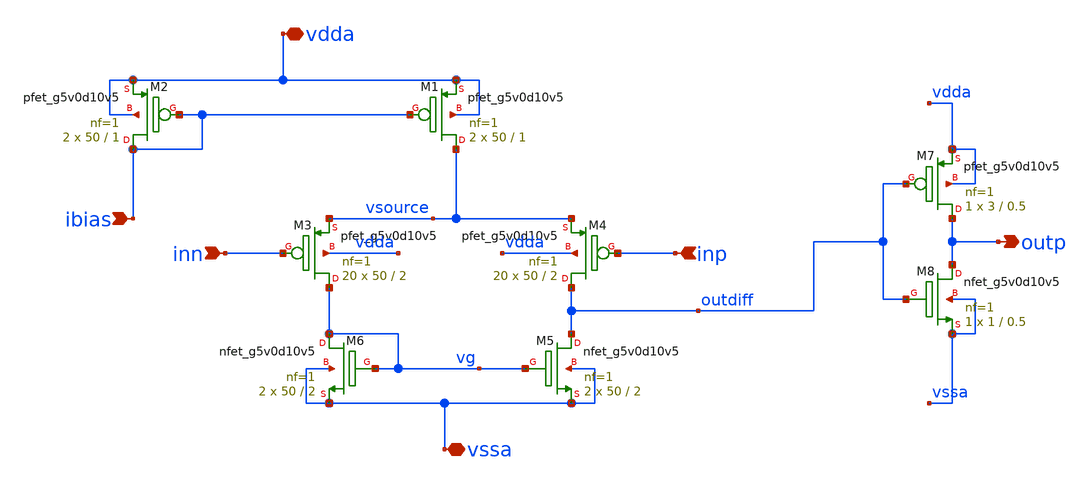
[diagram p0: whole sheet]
** sch_path: xschem/comparator1.sch
**.subckt comparator1 ibias inn inp vdda vssa outp
*.ipin ibias
*.ipin inn
*.ipin inp
*.iopin vdda
*.iopin vssa
*.opin outp
XM1 vsource ibias vdda vdda sky130_fd_pr__pfet_g5v0d10v5 L=1 W=50 nf=1 ad='int((nf+1)/2) * W/nf * 0.29'
+ as='int((nf+2)/2) * W/nf * 0.29' pd='2*int((nf+1)/2) * (W/nf + 0.29)' ps='2*int((nf+2)/2) * (W/nf + 0.29)'
+ nrd='0.29 / W' nrs='0.29 / W' sa=0 sb=0 sd=0 mult=2 m=2
XM2 ibias ibias vdda vdda sky130_fd_pr__pfet_g5v0d10v5 L=1 W=50 nf=1 ad='int((nf+1)/2) * W/nf * 0.29'
+ as='int((nf+2)/2) * W/nf * 0.29' pd='2*int((nf+1)/2) * (W/nf + 0.29)' ps='2*int((nf+2)/2) * (W/nf + 0.29)'
+ nrd='0.29 / W' nrs='0.29 / W' sa=0 sb=0 sd=0 mult=2 m=2
XM3 vg inn vsource vdda sky130_fd_pr__pfet_g5v0d10v5 L=2 W=50 nf=1 ad='int((nf+1)/2) * W/nf * 0.29' as='int((nf+2)/2) * W/nf * 0.29'
+ pd='2*int((nf+1)/2) * (W/nf + 0.29)' ps='2*int((nf+2)/2) * (W/nf + 0.29)' nrd='0.29 / W' nrs='0.29 / W'
+ sa=0 sb=0 sd=0 mult=20 m=20
XM4 outdiff inp vsource vdda sky130_fd_pr__pfet_g5v0d10v5 L=2 W=50 nf=1 ad='int((nf+1)/2) * W/nf * 0.29'
+ as='int((nf+2)/2) * W/nf * 0.29' pd='2*int((nf+1)/2) * (W/nf + 0.29)' ps='2*int((nf+2)/2) * (W/nf + 0.29)'
+ nrd='0.29 / W' nrs='0.29 / W' sa=0 sb=0 sd=0 mult=20 m=20
XM5 outdiff vg vssa vssa sky130_fd_pr__nfet_g5v0d10v5 L=2 W=50 nf=1 ad='int((nf+1)/2) * W/nf * 0.29'
+ as='int((nf+2)/2) * W/nf * 0.29' pd='2*int((nf+1)/2) * (W/nf + 0.29)' ps='2*int((nf+2)/2) * (W/nf + 0.29)'
+ nrd='0.29 / W' nrs='0.29 / W' sa=0 sb=0 sd=0 mult=2 m=2
XM6 vg vg vssa vssa sky130_fd_pr__nfet_g5v0d10v5 L=2 W=50 nf=1 ad='int((nf+1)/2) * W/nf * 0.29' as='int((nf+2)/2) * W/nf * 0.29'
+ pd='2*int((nf+1)/2) * (W/nf + 0.29)' ps='2*int((nf+2)/2) * (W/nf + 0.29)' nrd='0.29 / W' nrs='0.29 / W'
+ sa=0 sb=0 sd=0 mult=2 m=2
XM7 outp outdiff vdda vdda sky130_fd_pr__pfet_g5v0d10v5 L=0.5 W=3 nf=1 ad='int((nf+1)/2) * W/nf * 0.29'
+ as='int((nf+2)/2) * W/nf * 0.29' pd='2*int((nf+1)/2) * (W/nf + 0.29)' ps='2*int((nf+2)/2) * (W/nf + 0.29)'
+ nrd='0.29 / W' nrs='0.29 / W' sa=0 sb=0 sd=0 mult=1 m=1
XM8 outp outdiff vssa vssa sky130_fd_pr__nfet_g5v0d10v5 L=0.5 W=1 nf=1 ad='int((nf+1)/2) * W/nf * 0.29'
+ as='int((nf+2)/2) * W/nf * 0.29' pd='2*int((nf+1)/2) * (W/nf + 0.29)' ps='2*int((nf+2)/2) * (W/nf + 0.29)'
+ nrd='0.29 / W' nrs='0.29 / W' sa=0 sb=0 sd=0 mult=1 m=1
**.ends
.end
